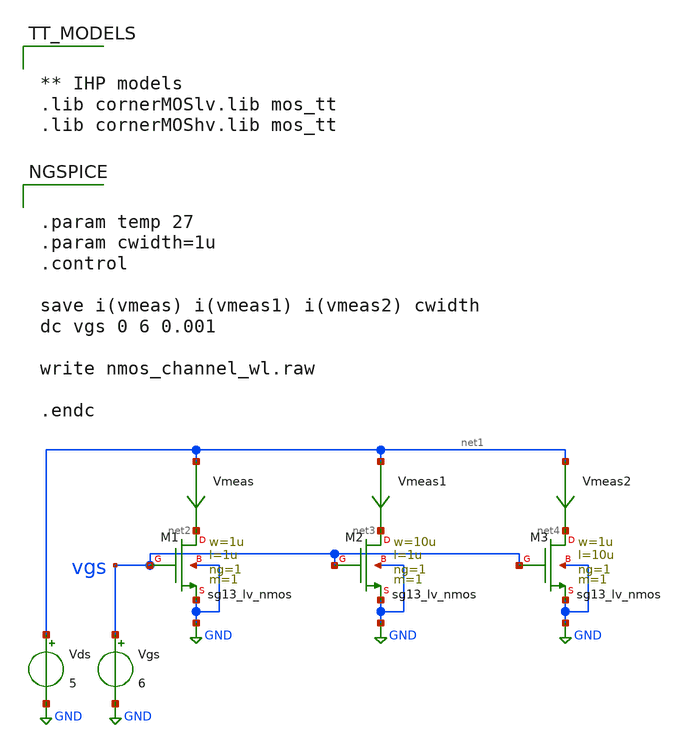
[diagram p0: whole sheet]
** sch_path: TempSensor/design_data/xschem/nmos_channel_wl.sch
**.subckt nmos_channel_wl
XM1 net2 vgs GND GND sg13_lv_nmos w=1u l=1u ng=1 m=1 mm_ok=1
Vgs vgs GND 6
XM2 net3 vgs GND GND sg13_lv_nmos w=10u l=1u ng=1 m=1 mm_ok=1
XM3 net4 vgs GND GND sg13_lv_nmos w=1u l=10u ng=1 m=1 mm_ok=1
Vds net1 GND 5
Vmeas net1 net2 0
.save i(vmeas)
Vmeas1 net1 net3 0
.save i(vmeas1)
Vmeas2 net1 net4 0
.save i(vmeas2)
**** begin user architecture code


.param temp 27
.param cwidth=1u
.control

save i(vmeas) i(vmeas1) i(vmeas2) cwidth
dc vgs 0 6 0.001

write nmos_channel_wl.raw

.endc




** IHP models
.lib cornerMOSlv.lib mos_tt
.lib cornerMOShv.lib mos_tt


**** end user architecture code
**.ends
.GLOBAL GND
.end
